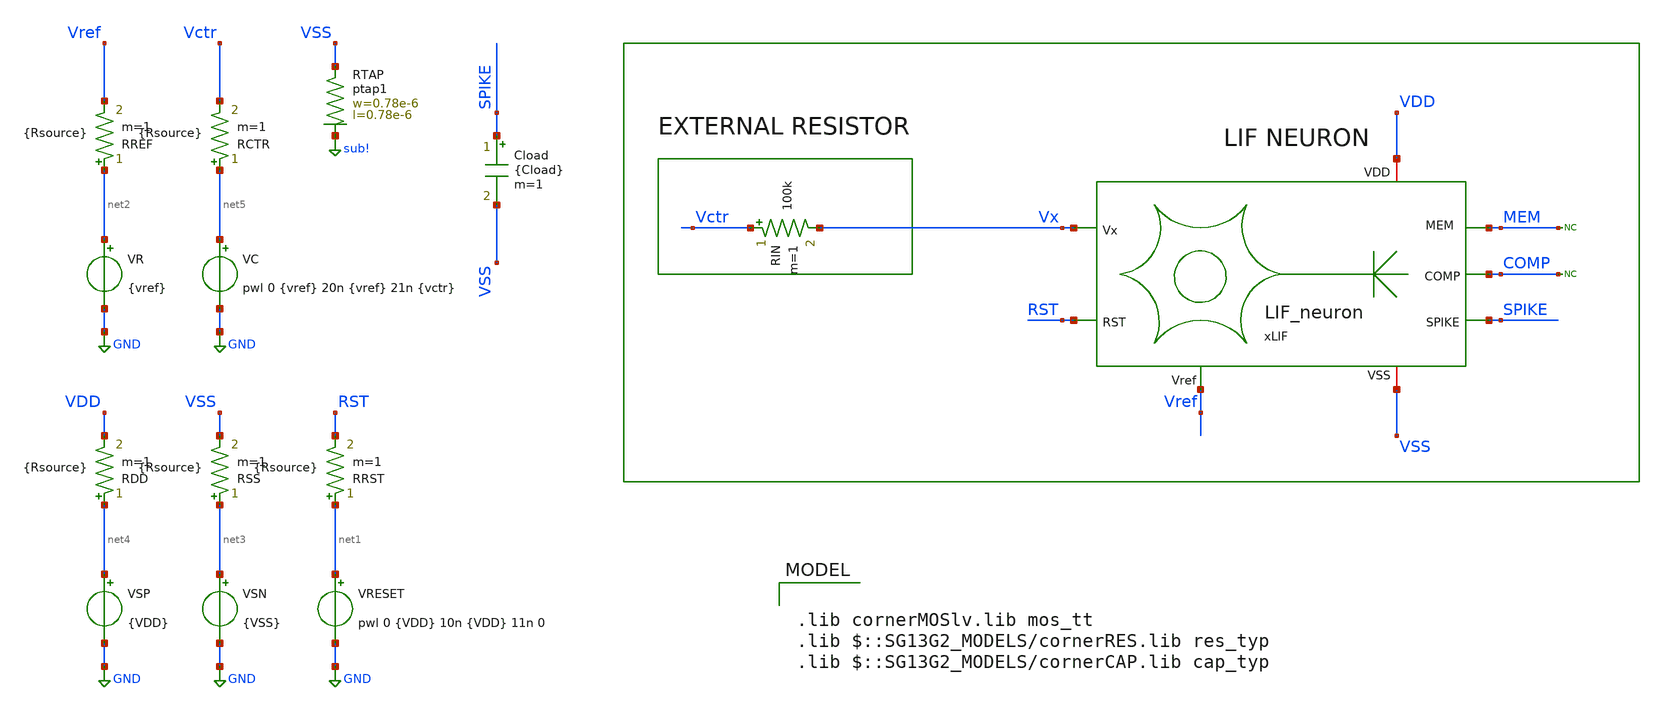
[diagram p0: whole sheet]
** sch_path: OSC9996-main/schematic/xschem/sweep_LIF_Neuron.sch
**.subckt sweep_LIF_Neuron
VRESET net1 GND pwl 0 {VDD} 10n {VDD} 11n 0
VSN net3 GND {VSS}
VR net2 GND {vref}
VC net5 GND pwl 0 {vref} 20n {vref} 21n {vctr}
xLIF VDD Vx MEM RST SPIKE VSS Vref COMP LIF_neuron
RDD net4 VDD {Rsource} m=1
RSS net3 VSS {Rsource} m=1
RRST net1 RST {Rsource} m=1
RREF net2 Vref {Rsource} m=1
RCTR net5 Vctr {Rsource} m=1
Cload SPIKE VSS {Cload} m=1
RIN Vctr Vx 100k m=1
VSP net4 GND {VDD}
* noconn MEM
XRTAP VSS sub! ptap1 R=262.8 w=0.78e-6 l=0.78e-6
* noconn COMP
**** begin user architecture code



.param VDD = 1.2
.param VSS = 0
.param vctr = 0.6
.param vref = 1.2
.param Cload = 0.1p
.param Rsource = 1m


.param sw_stat_global = 0
.param sw_stat_mismatch = 0

.save all

.control

* >> Variables <<

let Vhigh = 1.2
let Vmid = Vhigh * 0.5

let tstop = 0.1u
let tstep = tstop/2.5k

* Run transient analysis


=====================barrido===================

let VDD_start = 0
let VDD_end   = 1.2
let VDD_step  = 0.08

let idx = 0

let npoints = (VDD_end - VDD_start)/VDD_step
====================vectores===================

let VDD_vec = vector(npoints)
let spike_vec = vector(npoints)

settype voltage VDD_vec
settype voltage spike_vec

===============================================

let v = VDD_start

while v le VDD_end

  alterparam VDD = $&v

  reset
  tran 0.05n 50n

  meas tran SPIKE_max max v(SPIKE)

  let spike_vec[idx] = SPIKE_max
  let VDD_vec[idx] = v

  let v = v + VDD_step
  let idx = idx + 1

end

print v(spike_vec) v(VDD_vec)
plot spike_vec vs VDD_vec


.endc



.lib cornerMOSlv.lib mos_tt
.lib $::SG13G2_MODELS/cornerRES.lib res_typ
.lib $::SG13G2_MODELS/cornerCAP.lib cap_typ

**** end user architecture code
**.ends
.GLOBAL GND
.GLOBAL sub!
.end
